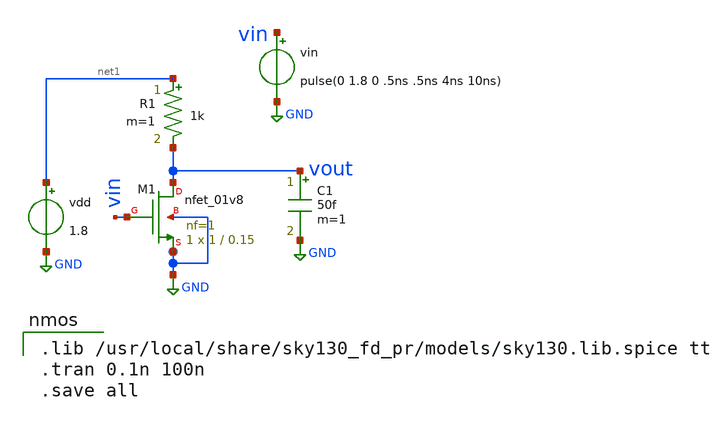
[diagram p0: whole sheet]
** sch_path: files/mos_characteristics/strong0_week1/nmos.sch
**.subckt nmos
XM1 vout vin GND GND sky130_fd_pr__nfet_01v8 L=0.15 W=1 nf=1 ad='int((1 + 1)/2) * 1 / 1 * 0.29' as='int((1 + 2)/2) * 1 / 1 * 0.29'
+ pd='2*int((1 + 1)/2) * (1 / 1 + 0.29)' ps='2*int((1 + 2)/2) * (1 / 1 + 0.29)' nrd='0.29 / 1 ' nrs='0.29 / 1 '
+ sa=0 sb=0 sd=0 mult=1 m=1
R1 net1 vout 1k m=1
C1 vout GND 50f m=1
vdd net1 GND 1.8
vin vin GND pulse(0 1.8 0 .5ns .5ns 4ns 10ns)
**** begin user architecture code

.lib /usr/local/share/sky130_fd_pr/models/sky130.lib.spice tt
.tran 0.1n 100n
.save all

**** end user architecture code
**.ends
.GLOBAL GND
.end
